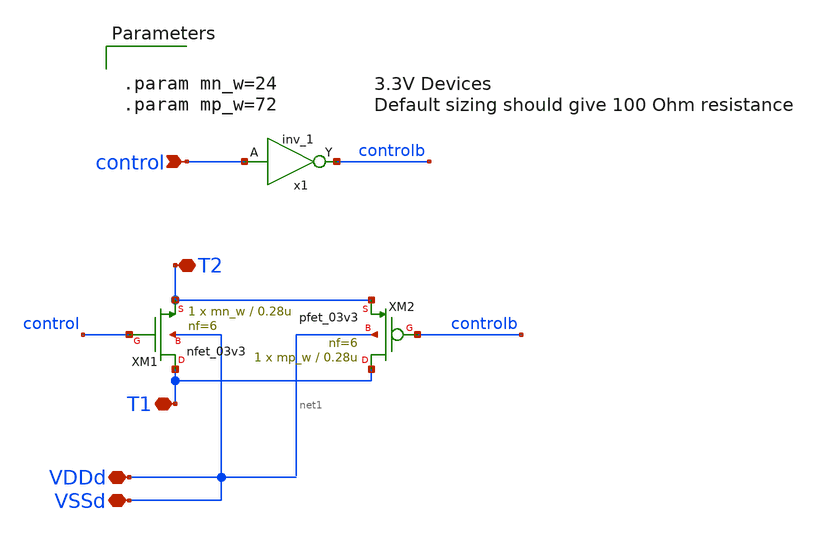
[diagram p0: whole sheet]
** sch_path: swmatrix_Tgate/swmatrix_Tgate.sch
**.subckt swmatrix_Tgate T1 T2 control VDDd VSSd
*.iopin T1
*.iopin T2
*.ipin control
*.iopin VDDd
*.iopin VSSd
XM1 T1 control T2 VDDd nfet_03v3 L=0.28u W=mn_w nf=6 ad='int((nf+1)/2) * W/nf * 0.18u' as='int((nf+2)/2) * W/nf * 0.18u'
+ pd='2*int((nf+1)/2) * (W/nf + 0.18u)' ps='2*int((nf+2)/2) * (W/nf + 0.18u)' nrd='0.18u / W' nrs='0.18u / W'
+ sa=0 sb=0 sd=0 m=1
XM2 T1 controlb T2 net1 pfet_03v3 L=0.28u W=mp_w nf=6 ad='int((nf+1)/2) * W/nf * 0.18u' as='int((nf+2)/2) * W/nf * 0.18u'
+ pd='2*int((nf+1)/2) * (W/nf + 0.18u)' ps='2*int((nf+2)/2) * (W/nf + 0.18u)' nrd='0.18u / W' nrs='0.18u / W'
+ sa=0 sb=0 sd=0 m=1
x1 control VSSd VDDd VSSd VDDd controlb gf180mcu_fd_sc_mcu9t5v0__inv_1
**** begin user architecture code


.param mn_w=24
.param mp_w=72

**** end user architecture code
**.ends
.end
